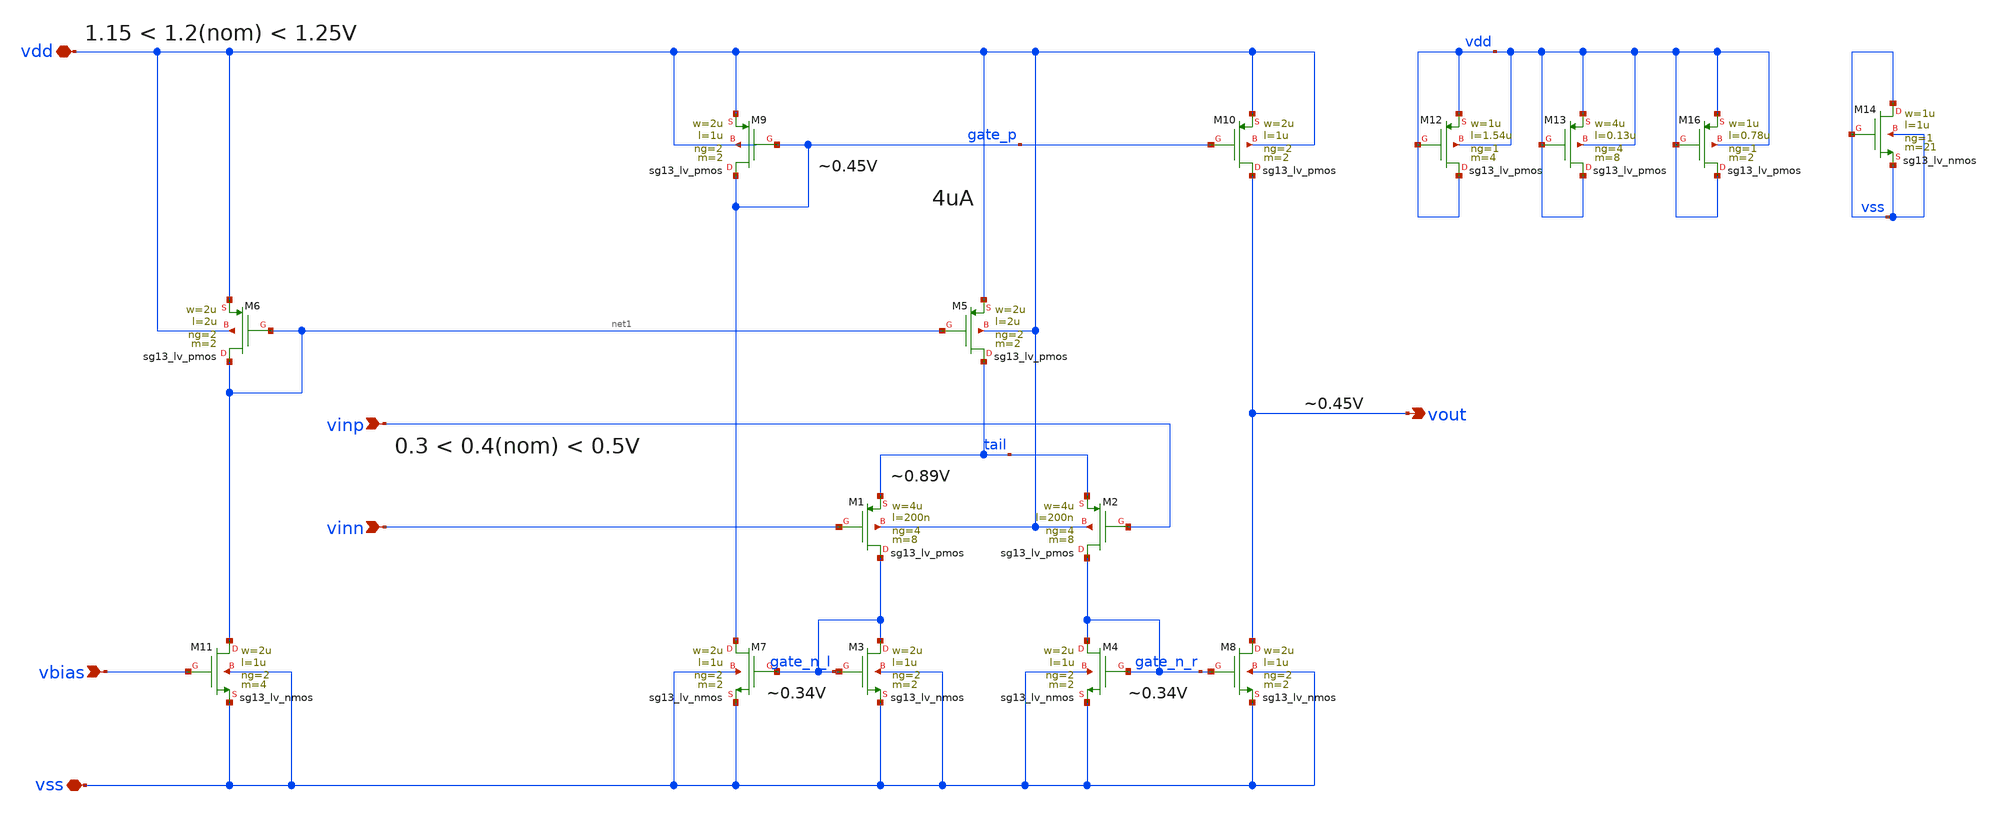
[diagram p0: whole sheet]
** sch_path: v2_feature_extr_withf/a_buffP.sch
* (c) 2026 Arianna Rubino, Apache-2.0 license
**.subckt a_buffP vinp vinn vbias vdd vss vout
*.ipin vinp
*.ipin vinn
*.ipin vbias
*.iopin vdd
*.iopin vss
*.opin vout
XM3 gate_n_l gate_n_l vss vss sg13_lv_nmos w=2u l=1u ng=2 m=2 mm_ok=1
XM1 gate_n_l vinn tail vdd sg13_lv_pmos w=4u l=200n ng=4 m=8 mm_ok=1
XM2 gate_n_r vinp tail vdd sg13_lv_pmos w=4u l=200n ng=4 m=8 mm_ok=1
XM5 tail net1 vdd vdd sg13_lv_pmos w=2u l=2u ng=2 m=2 mm_ok=1
XM4 gate_n_r gate_n_r vss vss sg13_lv_nmos w=2u l=1u ng=2 m=2 mm_ok=1
XM9 gate_p gate_p vdd vdd sg13_lv_pmos w=2u l=1u ng=2 m=2 mm_ok=1
XM10 vout gate_p vdd vdd sg13_lv_pmos w=2u l=1u ng=2 m=2 mm_ok=1
XM7 gate_p gate_n_l vss vss sg13_lv_nmos w=2u l=1u ng=2 m=2 mm_ok=1
XM8 vout gate_n_r vss vss sg13_lv_nmos w=2u l=1u ng=2 m=2 mm_ok=1
XM6 net1 net1 vdd vdd sg13_lv_pmos w=2u l=2u ng=2 m=2 mm_ok=1
XM11 net1 vbias vss vss sg13_lv_nmos w=2u l=1u ng=2 m=4 mm_ok=1
XM12 vdd vdd vdd vdd sg13_lv_pmos w=1u l=1.54u ng=1 m=4 mm_ok=1
XM13 vdd vdd vdd vdd sg13_lv_pmos w=4u l=0.13u ng=4 m=8 mm_ok=1
XM14 vss vss vss vss sg13_lv_nmos w=1u l=1u ng=1 m=21 mm_ok=1
XM16 vdd vdd vdd vdd sg13_lv_pmos w=1u l=0.78u ng=1 m=2 mm_ok=1
**.ends
.end
